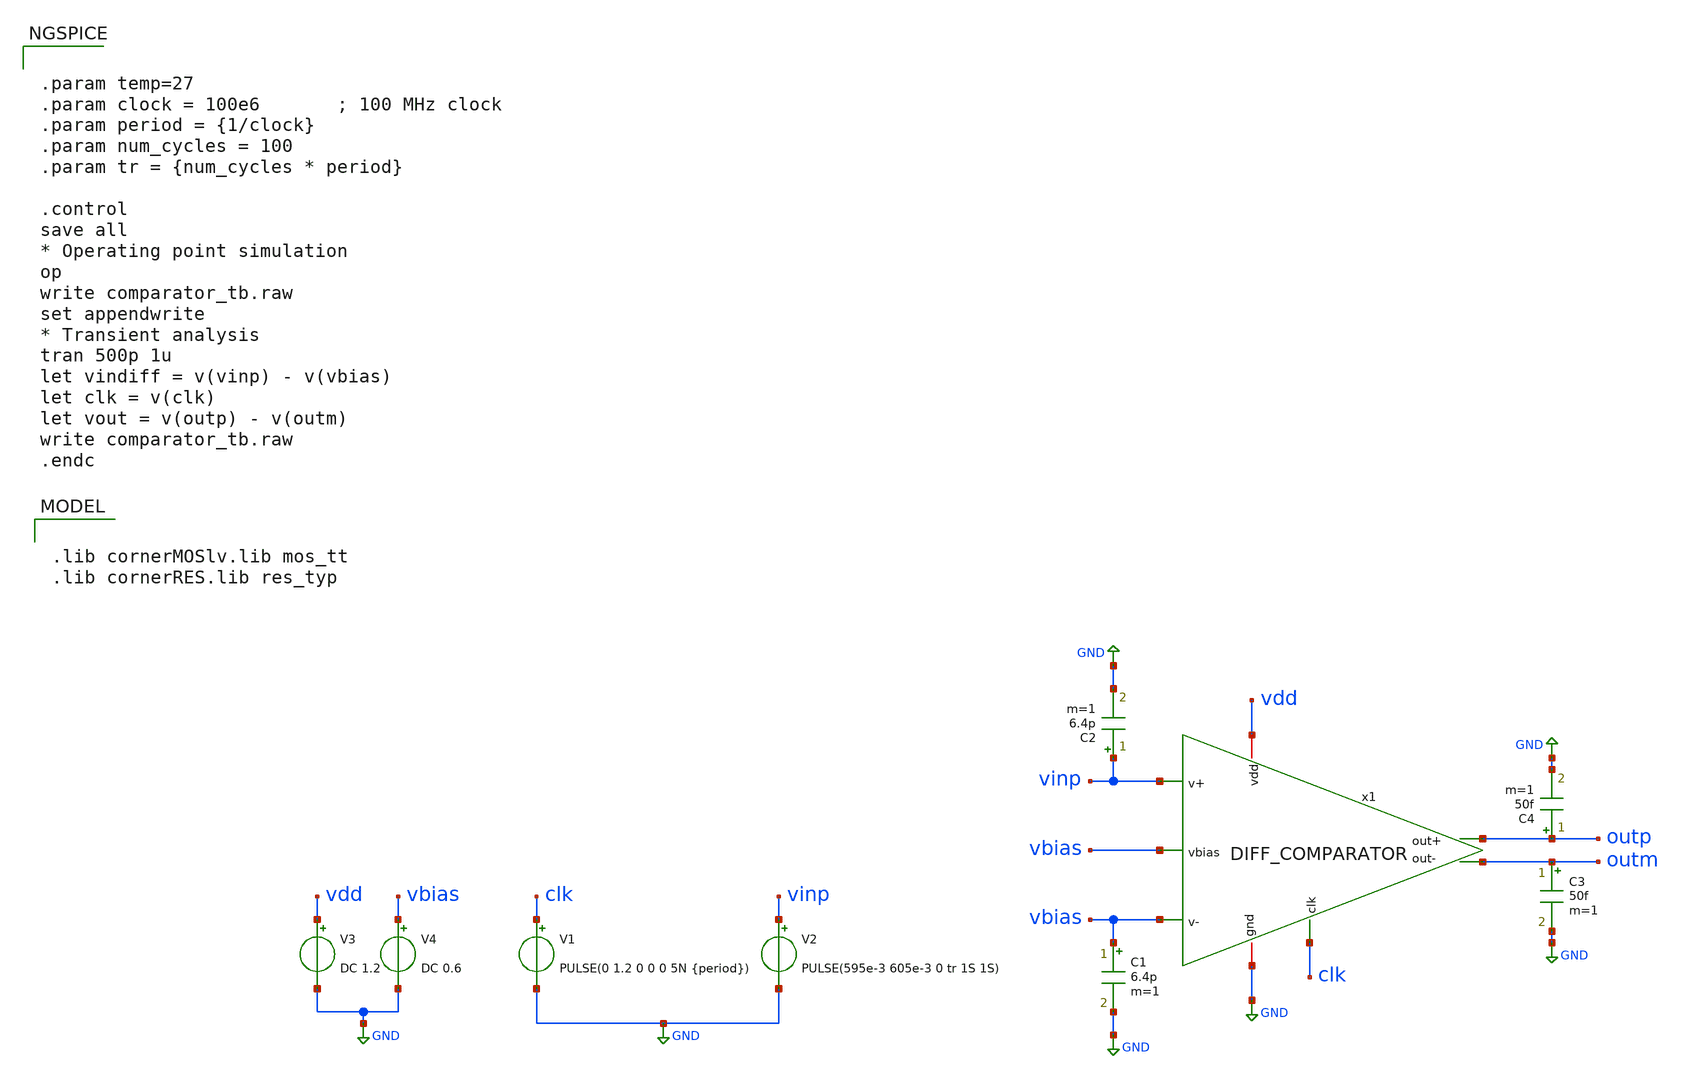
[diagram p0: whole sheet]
** sch_path: modules/module_3_8_bit_SAR_ADC/part_5_layout/comparator/xschem_post_layout/testbench/comparator_tb.sch
**.subckt comparator_tb
V3 vdd GND DC 1.2
V4 vbias GND DC 0.6
V1 clk GND PULSE(0 1.2 0 0 0 5N {period})
V2 vinp GND PULSE(595e-3 605e-3 0 tr 1S 1S)
C1 vbias GND 6.4p m=1
C2 vinp GND 6.4p m=1
C4 outp GND 50f m=1
C3 outm GND 50f m=1
x1 vdd vbias vinp vbias outm outp clk GND DIFF_COMPARATOR
**** begin user architecture code

.lib cornerMOSlv.lib mos_tt
.lib cornerRES.lib res_typ



.param temp=27
.param clock = 100e6       ; 100 MHz clock
.param period = {1/clock}
.param num_cycles = 100
.param tr = {num_cycles * period}

.control
save all
* Operating point simulation
op
write comparator_tb.raw
set appendwrite
* Transient analysis
tran 500p 1u
let vindiff = v(vinp) - v(vbias)
let clk = v(clk)
let vout = v(outp) - v(outm)
write comparator_tb.raw
.endc


**** end user architecture code
**.ends

* expanding   symbol:  DIFF_COMPARATOR.sym # of pins=8
** sym_path: modules/module_3_8_bit_SAR_ADC/part_5_layout/comparator/schematic/DIFF_COMPARATOR.sym
** sch_path: modules/module_3_8_bit_SAR_ADC/part_5_layout/comparator/schematic/DIFF_COMPARATOR.sch
.subckt DIFF_COMPARATOR vdd vbias v+ v- out- out+ clk gnd
*.iopin vdd
*.iopin gnd
*.ipin v+
*.ipin v-
*.ipin clk
*.opin out-
*.opin out+
*.ipin vbias
XM2 net3 v+ net1 well sg13_lv_pmos w=8u l=200n ng=2 m=4 mm_ok=1
XM1 net2 v- net1 well sg13_lv_pmos w=8u l=200n ng=2 m=4 mm_ok=1
XM4 out- net2 vdd well sg13_lv_pmos w=8u l=0.200u ng=2 m=1 mm_ok=1
XM5 out+ net3 vdd well sg13_lv_pmos w=8u l=0.200u ng=2 m=1 mm_ok=1
XM11 gnd net3 out+ sub sg13_lv_nmos w=4.0u l=0.200u ng=2 m=1 mm_ok=1
XM12 gnd net2 out- sub sg13_lv_nmos w=4.0u l=0.200u ng=2 m=1 mm_ok=1
XM6 gnd net2 net3 sub sg13_lv_nmos w=4.0u l=0.200u ng=1 m=1 mm_ok=1
XM10 gnd clk net3 sub sg13_lv_nmos w=4.0u l=0.200u ng=1 m=1 mm_ok=1
XM7 gnd clk net2 sub sg13_lv_nmos w=4.0u l=0.200u ng=1 m=1 mm_ok=1
XM8 gnd net3 net2 sub sg13_lv_nmos w=4.0u l=0.200u ng=1 m=1 mm_ok=1
XR1 vdd well ntap1 R=94.23m w=100e-6 l=100e-6
XM3 gnd gnd gnd sub sg13_lv_nmos w=4.0u l=0.200u ng=1 m=4 mm_ok=1
XR2 gnd sub ptap1 R=94.23m w=100e-6 l=100e-6
XM13 net1 clk net4 well sg13_lv_pmos w=18u l=0.3u ng=4 m=1 mm_ok=1
XM9 net4 vbias vdd well sg13_lv_pmos w=18u l=0.3u ng=4 m=1 mm_ok=1
.ends

.GLOBAL GND
.end
